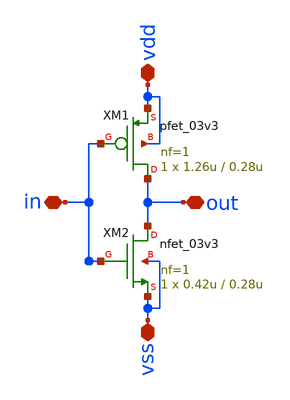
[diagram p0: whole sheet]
** sch_path: samples/inv_sample/symbol/inv_sample.sch
**.subckt inv_sample vdd out vss in
*.iopin vdd
*.iopin out
*.iopin vss
*.iopin in
XM1 out in vdd vdd pfet_03v3 L=0.28u W=1.26u nf=1 ad='int((nf+1)/2) * W/nf * 0.18u' as='int((nf+2)/2) * W/nf * 0.18u'
+ pd='2*int((nf+1)/2) * (W/nf + 0.18u)' ps='2*int((nf+2)/2) * (W/nf + 0.18u)' nrd='0.18u / W' nrs='0.18u / W'
+ sa=0 sb=0 sd=0 m=1
XM2 out in vss vss nfet_03v3 L=0.28u W=0.42u nf=1 ad='int((nf+1)/2) * W/nf * 0.18u' as='int((nf+2)/2) * W/nf * 0.18u'
+ pd='2*int((nf+1)/2) * (W/nf + 0.18u)' ps='2*int((nf+2)/2) * (W/nf + 0.18u)' nrd='0.18u / W' nrs='0.18u / W'
+ sa=0 sb=0 sd=0 m=1
**.ends
.end
